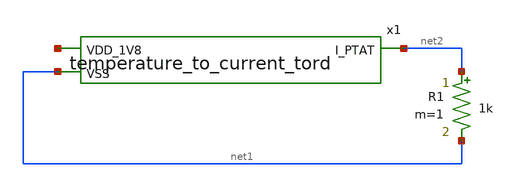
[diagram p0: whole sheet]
** sch_path: design/JNW_GR07_SKY130A/temperature_to_current_tord_tb.sch
**.subckt temperature_to_current_tord_tb
x1 net3 net2 net1 temperature_to_current_tord
R1 net2 net1 1k m=1
**.ends
.end
